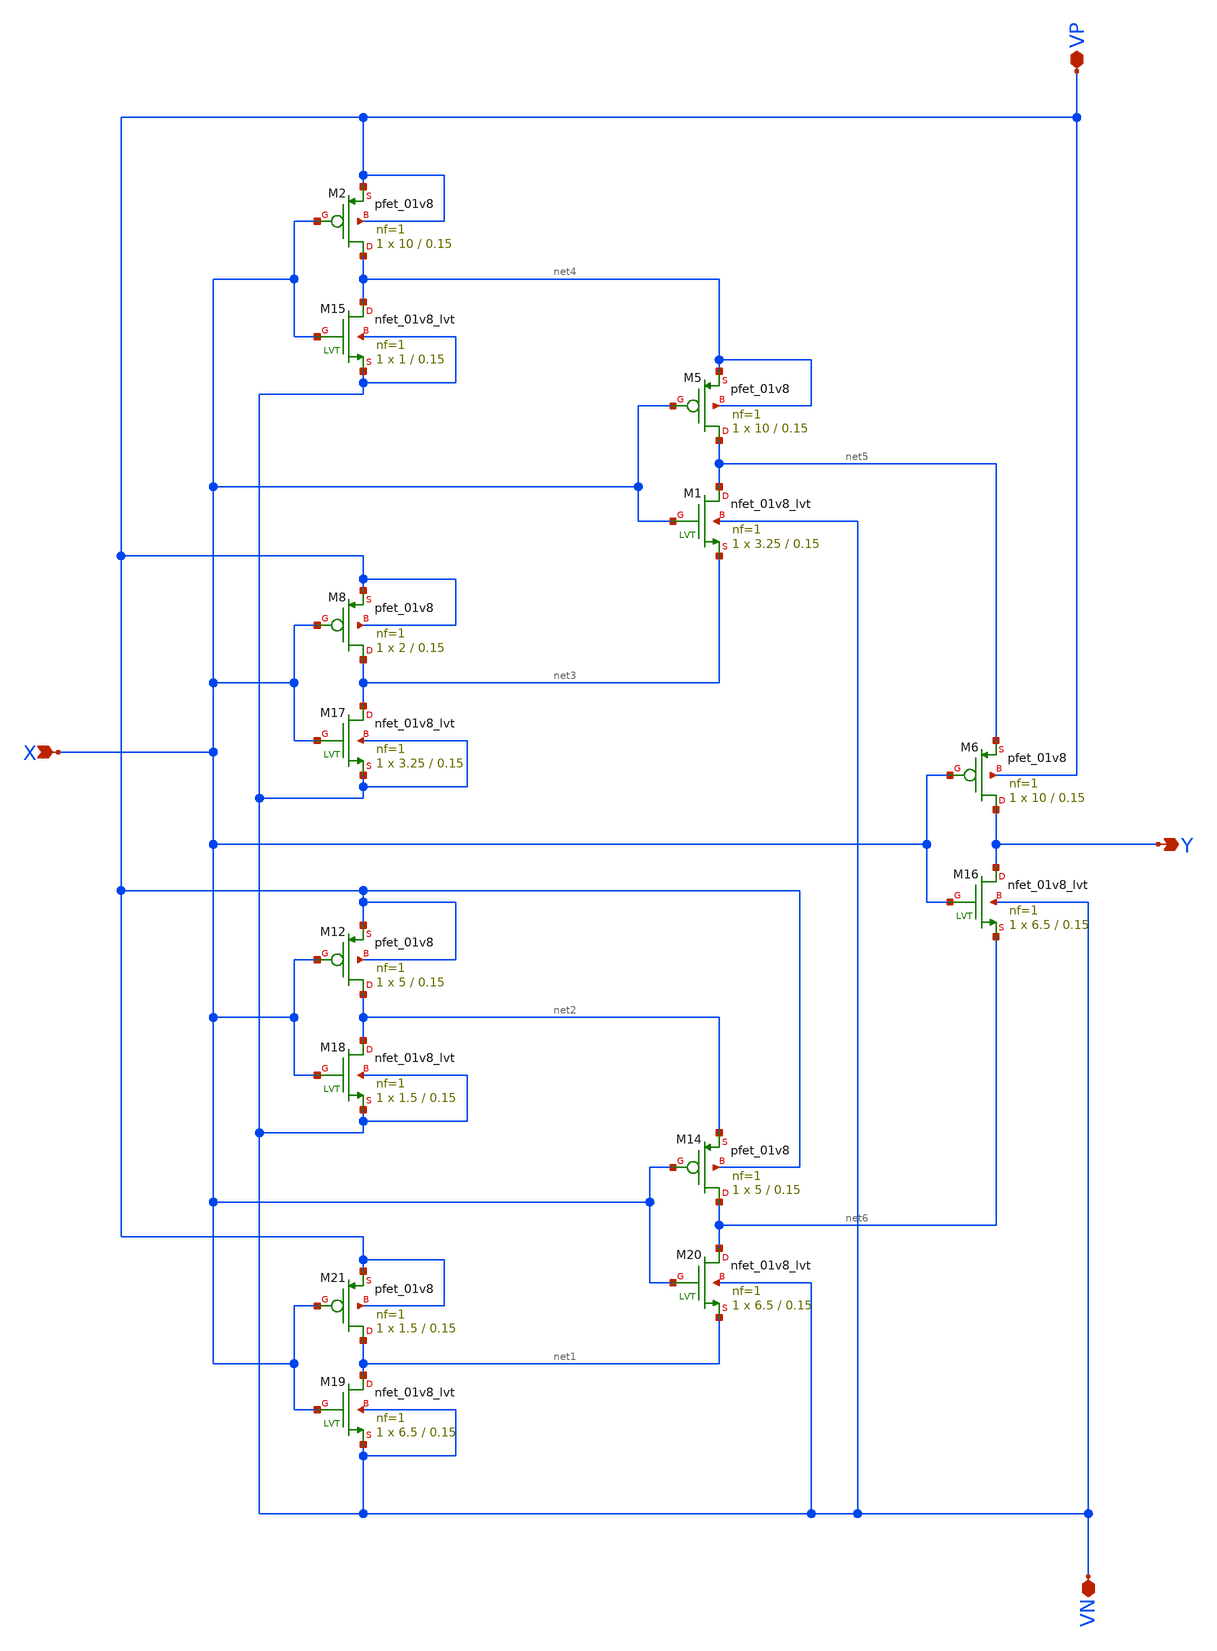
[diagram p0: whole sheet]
** sch_path: component/Reduntant_Inverter/Redn_INV.sch
**.subckt Redn_INV Y X VP VN
*.opin Y
*.ipin X
*.iopin VP
*.iopin VN
XM15 net4 X VN VN sky130_fd_pr__nfet_01v8_lvt L=0.15 W=1 nf=1 ad='int((nf+1)/2) * W/nf * 0.29' as='int((nf+2)/2) * W/nf * 0.29'
+ pd='2*int((nf+1)/2) * (W/nf + 0.29)' ps='2*int((nf+2)/2) * (W/nf + 0.29)' nrd='0.29 / W' nrs='0.29 / W'
+ sa=0 sb=0 sd=0 mult=1 m=1
XM1 net5 X net3 VN sky130_fd_pr__nfet_01v8_lvt L=0.15 W=3.25 nf=1 ad='int((nf+1)/2) * W/nf * 0.29' as='int((nf+2)/2) * W/nf * 0.29'
+ pd='2*int((nf+1)/2) * (W/nf + 0.29)' ps='2*int((nf+2)/2) * (W/nf + 0.29)' nrd='0.29 / W' nrs='0.29 / W'
+ sa=0 sb=0 sd=0 mult=1 m=1
XM16 Y X net6 VN sky130_fd_pr__nfet_01v8_lvt L=0.15 W=6.5 nf=1 ad='int((nf+1)/2) * W/nf * 0.29' as='int((nf+2)/2) * W/nf * 0.29'
+ pd='2*int((nf+1)/2) * (W/nf + 0.29)' ps='2*int((nf+2)/2) * (W/nf + 0.29)' nrd='0.29 / W' nrs='0.29 / W'
+ sa=0 sb=0 sd=0 mult=1 m=1
XM17 net3 X VN VN sky130_fd_pr__nfet_01v8_lvt L=0.15 W=3.25 nf=1 ad='int((nf+1)/2) * W/nf * 0.29' as='int((nf+2)/2) * W/nf * 0.29'
+ pd='2*int((nf+1)/2) * (W/nf + 0.29)' ps='2*int((nf+2)/2) * (W/nf + 0.29)' nrd='0.29 / W' nrs='0.29 / W'
+ sa=0 sb=0 sd=0 mult=1 m=1
XM18 net2 X VN VN sky130_fd_pr__nfet_01v8_lvt L=0.15 W=1.5 nf=1 ad='int((nf+1)/2) * W/nf * 0.29' as='int((nf+2)/2) * W/nf * 0.29'
+ pd='2*int((nf+1)/2) * (W/nf + 0.29)' ps='2*int((nf+2)/2) * (W/nf + 0.29)' nrd='0.29 / W' nrs='0.29 / W'
+ sa=0 sb=0 sd=0 mult=1 m=1
XM19 net1 X VN VN sky130_fd_pr__nfet_01v8_lvt L=0.15 W=6.5 nf=1 ad='int((nf+1)/2) * W/nf * 0.29' as='int((nf+2)/2) * W/nf * 0.29'
+ pd='2*int((nf+1)/2) * (W/nf + 0.29)' ps='2*int((nf+2)/2) * (W/nf + 0.29)' nrd='0.29 / W' nrs='0.29 / W'
+ sa=0 sb=0 sd=0 mult=1 m=1
XM20 net6 X net1 VN sky130_fd_pr__nfet_01v8_lvt L=0.15 W=6.5 nf=1 ad='int((nf+1)/2) * W/nf * 0.29' as='int((nf+2)/2) * W/nf * 0.29'
+ pd='2*int((nf+1)/2) * (W/nf + 0.29)' ps='2*int((nf+2)/2) * (W/nf + 0.29)' nrd='0.29 / W' nrs='0.29 / W'
+ sa=0 sb=0 sd=0 mult=1 m=1
XM2 net4 X VP VP sky130_fd_pr__pfet_01v8 L=0.15 W=10 nf=1 ad='int((nf+1)/2) * W/nf * 0.29' as='int((nf+2)/2) * W/nf * 0.29'
+ pd='2*int((nf+1)/2) * (W/nf + 0.29)' ps='2*int((nf+2)/2) * (W/nf + 0.29)' nrd='0.29 / W' nrs='0.29 / W'
+ sa=0 sb=0 sd=0 mult=1 m=1
XM5 net5 X net4 net4 sky130_fd_pr__pfet_01v8 L=0.15 W=10 nf=1 ad='int((nf+1)/2) * W/nf * 0.29' as='int((nf+2)/2) * W/nf * 0.29'
+ pd='2*int((nf+1)/2) * (W/nf + 0.29)' ps='2*int((nf+2)/2) * (W/nf + 0.29)' nrd='0.29 / W' nrs='0.29 / W'
+ sa=0 sb=0 sd=0 mult=1 m=1
XM6 Y X net5 VP sky130_fd_pr__pfet_01v8 L=0.15 W=10 nf=1 ad='int((nf+1)/2) * W/nf * 0.29' as='int((nf+2)/2) * W/nf * 0.29'
+ pd='2*int((nf+1)/2) * (W/nf + 0.29)' ps='2*int((nf+2)/2) * (W/nf + 0.29)' nrd='0.29 / W' nrs='0.29 / W'
+ sa=0 sb=0 sd=0 mult=1 m=1
XM8 net3 X VP VP sky130_fd_pr__pfet_01v8 L=0.15 W=2 nf=1 ad='int((nf+1)/2) * W/nf * 0.29' as='int((nf+2)/2) * W/nf * 0.29'
+ pd='2*int((nf+1)/2) * (W/nf + 0.29)' ps='2*int((nf+2)/2) * (W/nf + 0.29)' nrd='0.29 / W' nrs='0.29 / W'
+ sa=0 sb=0 sd=0 mult=1 m=1
XM12 net2 X VP VP sky130_fd_pr__pfet_01v8 L=0.15 W=5 nf=1 ad='int((nf+1)/2) * W/nf * 0.29' as='int((nf+2)/2) * W/nf * 0.29'
+ pd='2*int((nf+1)/2) * (W/nf + 0.29)' ps='2*int((nf+2)/2) * (W/nf + 0.29)' nrd='0.29 / W' nrs='0.29 / W'
+ sa=0 sb=0 sd=0 mult=1 m=1
XM14 net6 X net2 VP sky130_fd_pr__pfet_01v8 L=0.15 W=5 nf=1 ad='int((nf+1)/2) * W/nf * 0.29' as='int((nf+2)/2) * W/nf * 0.29'
+ pd='2*int((nf+1)/2) * (W/nf + 0.29)' ps='2*int((nf+2)/2) * (W/nf + 0.29)' nrd='0.29 / W' nrs='0.29 / W'
+ sa=0 sb=0 sd=0 mult=1 m=1
XM21 net1 X VP VP sky130_fd_pr__pfet_01v8 L=0.15 W=1.5 nf=1 ad='int((nf+1)/2) * W/nf * 0.29' as='int((nf+2)/2) * W/nf * 0.29'
+ pd='2*int((nf+1)/2) * (W/nf + 0.29)' ps='2*int((nf+2)/2) * (W/nf + 0.29)' nrd='0.29 / W' nrs='0.29 / W'
+ sa=0 sb=0 sd=0 mult=1 m=1
**.ends
.end
